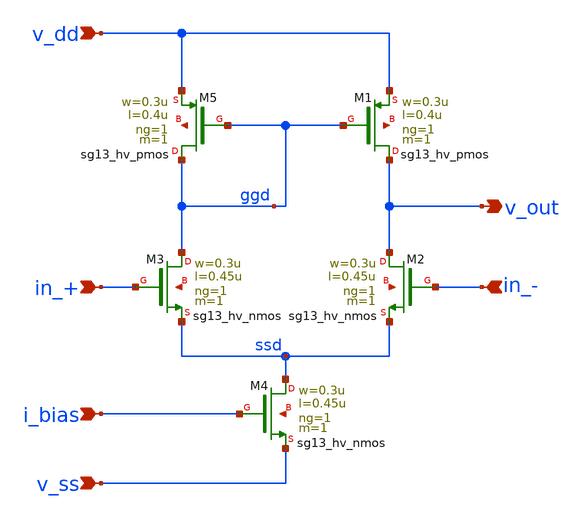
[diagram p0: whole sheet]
** sch_path: 3_Real_Cir/self_build_opamp.sch
**.subckt self_build_opamp in_+ in_- v_ss v_dd i_bias v_out
*.ipin in_+
*.ipin in_-
*.ipin v_ss
*.ipin v_dd
*.ipin i_bias
*.opin v_out
XM3 ggd in_+ ssd net1 sg13_hv_nmos w=0.3u l=0.45u ng=1 m=1 mm_ok=1
XM2 v_out in_- ssd net2 sg13_hv_nmos w=0.3u l=0.45u ng=1 m=1 mm_ok=1
XM4 ssd i_bias v_ss net3 sg13_hv_nmos w=0.3u l=0.45u ng=1 m=1 mm_ok=1
XM5 ggd ggd v_dd net4 sg13_hv_pmos w=0.3u l=0.4u ng=1 m=1 mm_ok=1
XM1 v_out ggd v_dd net5 sg13_hv_pmos w=0.3u l=0.4u ng=1 m=1 mm_ok=1
**.ends
.end
